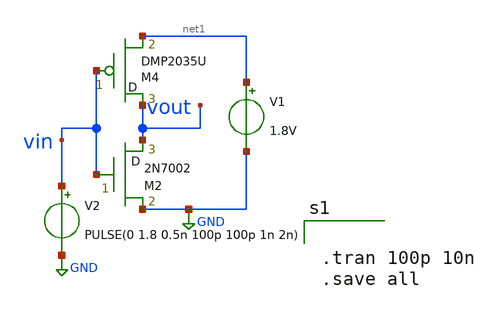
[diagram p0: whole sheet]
** sch_path: inv_testt.sch
**.subckt inv_testt
V1 net1 GND 1.8V
V2 vin GND PULSE(0 1.8 0.5n 100p 100p 1n 2n)
M2 vout vin GND M2N7002 m=1
M4 vout vin net1 DMP2035U m=1
**** begin user architecture code


.tran 100p 10n
.save all

**** end user architecture code
**.ends
.GLOBAL GND
.end
